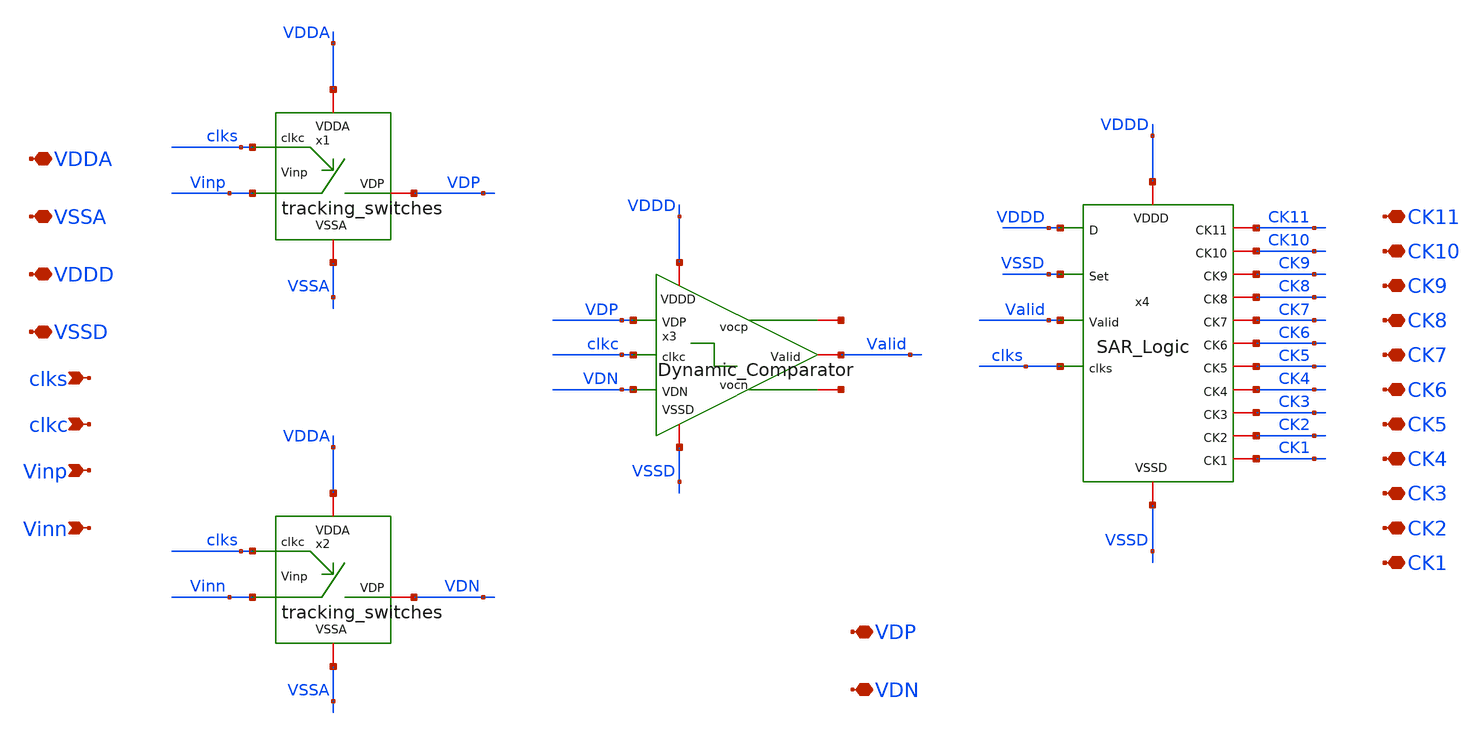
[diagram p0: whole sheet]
** sch_path: SAR_ADC/integration/TrackingSW_DynComp_SARLogic_bkp.sch
**.subckt TrackingSW_DynComp_SARLogic_bkp VDDD VSSD clks VDDA VSSA clkc Vinp Vinn VDP VDN CK11 CK10
*+ CK9 CK8 CK7 CK6 CK5 CK4 CK3 CK2 CK1
*.iopin VDDD
*.iopin VSSD
*.ipin clks
*.iopin VDDA
*.iopin VSSA
*.ipin clkc
*.ipin Vinp
*.ipin Vinn
*.iopin VDP
*.iopin VDN
*.iopin CK11
*.iopin CK10
*.iopin CK9
*.iopin CK8
*.iopin CK7
*.iopin CK6
*.iopin CK5
*.iopin CK4
*.iopin CK3
*.iopin CK2
*.iopin CK1
x1 VDP VDDA VSSA clks Vinp tracking_switches
x2 VDN VDDA VSSA clks Vinn tracking_switches
x3 net1 net2 VDDD VSSD VDP VDN Valid clkc Dynamic_Comparator
x4 CK11 VDDD CK1 CK6 VSSD CK10 CK5 CK9 CK4 clks CK8 CK3 Valid CK2 CK7 VSSD VDDD SAR_Logic
**.ends
.end
